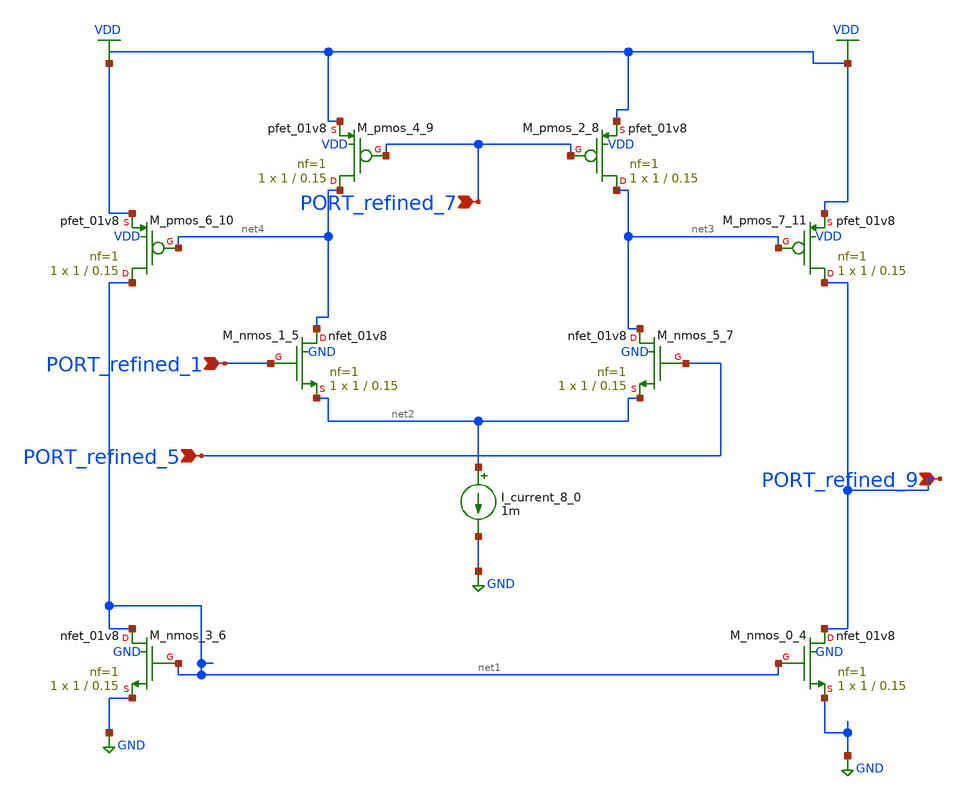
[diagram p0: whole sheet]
** sch_path: schematics/10_11648_j_ajpa_20241201_12_03_003.sch
**.subckt 10_11648_j_ajpa_20241201_12_03_003 PORT_refined_1 PORT_refined_9 PORT_refined_5
*+ PORT_refined_7
*.ipin PORT_refined_1
*.ipin PORT_refined_9
*.ipin PORT_refined_5
*.ipin PORT_refined_7
I_current_8_0 net2 GND 1m
XM_nmos_0_4 PORT_refined_9 net1 GND GND sky130_fd_pr__nfet_01v8 L=0.15 W=1 nf=1 ad='int((1 + 1)/2) * 1 / 1 * 0.29'
+ as='int((1 + 2)/2) * 1 / 1 * 0.29' pd='2*int((1 + 1)/2) * (1 / 1 + 0.29)' ps='2*int((1 + 2)/2) * (1 / 1 + 0.29)'
+ nrd='0.29 / 1 ' nrs='0.29 / 1 ' sa=0 sb=0 sd=0 mult=1 m=1
XM_nmos_1_5 net4 PORT_refined_1 net2 GND sky130_fd_pr__nfet_01v8 L=0.15 W=1 nf=1 ad='int((1 + 1)/2) * 1 / 1 * 0.29'
+ as='int((1 + 2)/2) * 1 / 1 * 0.29' pd='2*int((1 + 1)/2) * (1 / 1 + 0.29)' ps='2*int((1 + 2)/2) * (1 / 1 + 0.29)'
+ nrd='0.29 / 1 ' nrs='0.29 / 1 ' sa=0 sb=0 sd=0 mult=1 m=1
XM_nmos_3_6 net1 net1 GND GND sky130_fd_pr__nfet_01v8 L=0.15 W=1 nf=1 ad='int((1 + 1)/2) * 1 / 1 * 0.29'
+ as='int((1 + 2)/2) * 1 / 1 * 0.29' pd='2*int((1 + 1)/2) * (1 / 1 + 0.29)' ps='2*int((1 + 2)/2) * (1 / 1 + 0.29)'
+ nrd='0.29 / 1 ' nrs='0.29 / 1 ' sa=0 sb=0 sd=0 mult=1 m=1
XM_nmos_5_7 net3 PORT_refined_5 net2 GND sky130_fd_pr__nfet_01v8 L=0.15 W=1 nf=1 ad='int((1 + 1)/2) * 1 / 1 * 0.29'
+ as='int((1 + 2)/2) * 1 / 1 * 0.29' pd='2*int((1 + 1)/2) * (1 / 1 + 0.29)' ps='2*int((1 + 2)/2) * (1 / 1 + 0.29)'
+ nrd='0.29 / 1 ' nrs='0.29 / 1 ' sa=0 sb=0 sd=0 mult=1 m=1
XM_pmos_2_8 net3 PORT_refined_7 VDD VDD sky130_fd_pr__pfet_01v8 L=0.15 W=1 nf=1 ad='int((1 + 1)/2) * 1 / 1 * 0.29'
+ as='int((1 + 2)/2) * 1 / 1 * 0.29' pd='2*int((1 + 1)/2) * (1 / 1 + 0.29)' ps='2*int((1 + 2)/2) * (1 / 1 + 0.29)'
+ nrd='0.29 / 1 ' nrs='0.29 / 1 ' sa=0 sb=0 sd=0 mult=1 m=1
XM_pmos_4_9 net4 PORT_refined_7 VDD VDD sky130_fd_pr__pfet_01v8 L=0.15 W=1 nf=1 ad='int((1 + 1)/2) * 1 / 1 * 0.29'
+ as='int((1 + 2)/2) * 1 / 1 * 0.29' pd='2*int((1 + 1)/2) * (1 / 1 + 0.29)' ps='2*int((1 + 2)/2) * (1 / 1 + 0.29)'
+ nrd='0.29 / 1 ' nrs='0.29 / 1 ' sa=0 sb=0 sd=0 mult=1 m=1
XM_pmos_6_10 net1 net4 VDD VDD sky130_fd_pr__pfet_01v8 L=0.15 W=1 nf=1 ad='int((1 + 1)/2) * 1 / 1 * 0.29'
+ as='int((1 + 2)/2) * 1 / 1 * 0.29' pd='2*int((1 + 1)/2) * (1 / 1 + 0.29)' ps='2*int((1 + 2)/2) * (1 / 1 + 0.29)'
+ nrd='0.29 / 1 ' nrs='0.29 / 1 ' sa=0 sb=0 sd=0 mult=1 m=1
XM_pmos_7_11 PORT_refined_9 net3 VDD VDD sky130_fd_pr__pfet_01v8 L=0.15 W=1 nf=1 ad='int((1 + 1)/2) * 1 / 1 * 0.29'
+ as='int((1 + 2)/2) * 1 / 1 * 0.29' pd='2*int((1 + 1)/2) * (1 / 1 + 0.29)' ps='2*int((1 + 2)/2) * (1 / 1 + 0.29)'
+ nrd='0.29 / 1 ' nrs='0.29 / 1 ' sa=0 sb=0 sd=0 mult=1 m=1
**.ends
.GLOBAL GND
.GLOBAL VDD
.end
